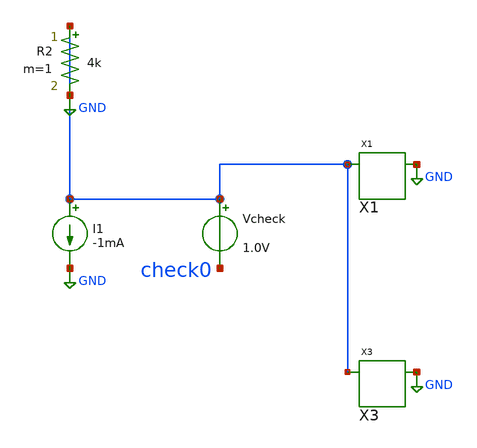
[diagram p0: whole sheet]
** sch_path: data/sch/aicas_ex1b.sch
**.subckt aicas_ex1b
I1 GND GND -1mA
X1 GND GND sub1
R2 GND GND 4k m=1
X3 GND GND sub_in_lib
Vcheck GND check0 1.0V
**.ends
.GLOBAL GND
.end
